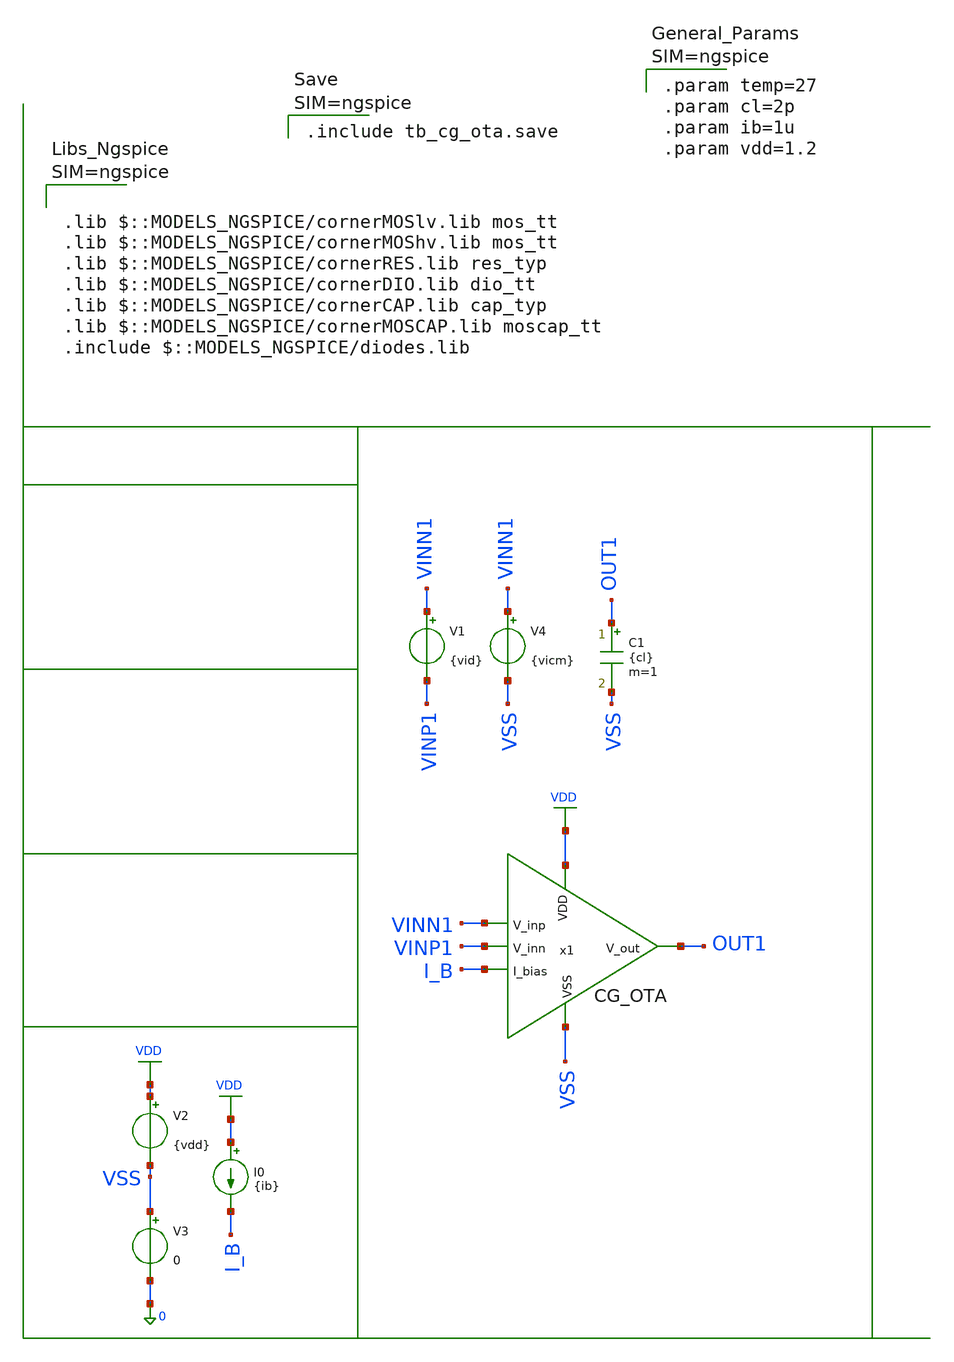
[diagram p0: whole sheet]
** sch_path: designs/libs/tb_analog/tb_cg_ota/tb_cg_ota.sch
**.subckt tb_cg_ota
x1 VDD VINN1 VINP1 OUT1 I_B VSS cg_ota
V1 VINN1 VINP1 {vid}
I0 VDD I_B {ib}
V2 VDD VSS {vdd}
V3 VSS 0 0
V4 VINN1 VSS {vicm}
C1 OUT1 VSS {cl} m=1
**** begin user architecture code


.param temp=27
.param cl=2p
.param ib=1u
.param vdd=1.2





.param vid=0
.param vicm=0.6
.op
.control
save all
op
shell mkdir -p result
run
write ./result/tb_cg_ota_op.raw
show all : vgs, vds, vth
let i_q = -i(v2)
let p_q = i_q * 1.2
let p_q_uw = p_q * 1e6
let i_q_ua = i_q * 1e6
echo "======================================================="
echo " Quiescent Current (I_q): " $&i_q_ua " uA"
echo " Quiescent Power (P_q): " $&p_q_uw " uW"
echo "======================================================="
.endc





.include tb_cg_ota.save







.lib $::MODELS_NGSPICE/cornerMOSlv.lib mos_tt
.lib $::MODELS_NGSPICE/cornerMOShv.lib mos_tt
.lib $::MODELS_NGSPICE/cornerRES.lib res_typ
.lib $::MODELS_NGSPICE/cornerDIO.lib dio_tt
.lib $::MODELS_NGSPICE/cornerCAP.lib cap_typ
.lib $::MODELS_NGSPICE/cornerMOSCAP.lib moscap_tt
.include $::MODELS_NGSPICE/diodes.lib





.param vid=0
.param vicm=0.6
.op
.control
save all
op
shell mkdir -p result
run
write ./result/tb_cg_ota_op.raw
show all : vgs, vds, vth
let i_q = -i(v2)
let p_q = i_q * 1.2
let p_q_uw = p_q * 1e6
let i_q_ua = i_q * 1e6
echo "======================================================="
echo " Quiescent Current (I_q): " $&i_q_ua " uA"
echo " Quiescent Power (P_q): " $&p_q_uw " uW"
echo "======================================================="
.endc





.param vid=0
.param vicm=0.6
.op
.control
save all
op
shell mkdir -p result
run
write ./result/tb_cg_ota_op.raw
show all : vgs, vds, vth
let i_q = -i(v2)
let p_q = i_q * 1.2
let p_q_uw = p_q * 1e6
let i_q_ua = i_q * 1e6
echo "======================================================="
echo " Quiescent Current (I_q): " $&i_q_ua " uA"
echo " Quiescent Power (P_q): " $&p_q_uw " uW"
echo "======================================================="
.endc



**** end user architecture code
**.ends

* expanding   symbol:
*+  /foss/designs/Programmable-Instrumentation-Amplifier-IP/designs/libs/core_analog/coarse_gain/cg_ota.sym # of pins=6
** sym_path: designs/libs/core_analog/coarse_gain/cg_ota.sym
** sch_path: designs/libs/core_analog/coarse_gain/cg_ota.sch
.subckt cg_ota VDD V_inp V_inn V_out I_bias VSS
*.ipin V_inp
*.ipin VDD
*.ipin VSS
*.opin V_out
*.ipin I_bias
*.ipin V_inn
XM1 F1 V_inp net7 net8 sg13_lv_pmos w=26.56u l=2u ng=4 m=1 mm_ok=1
XM2 F2 V_inn net7 net8 sg13_lv_pmos w=26.56u l=2u ng=4 m=1 mm_ok=1
XM3 net1 net1 VDD VDD sg13_lv_pmos w=7.33u l=2u ng=1 m=1 mm_ok=1
XM4 N_A net1 VDD VDD sg13_lv_pmos w=7.33u l=2u ng=1 m=1 mm_ok=1
XM7 F1 V_bn2 VSS VSS sg13_lv_nmos w=9.21u l=2u ng=1 m=1 mm_ok=1
XM8 F2 V_bn2 VSS VSS sg13_lv_nmos w=9.21u l=2u ng=1 m=1 mm_ok=1
XM_tail net7 V_btail VDD VDD sg13_lv_pmos w=5.33u l=2u ng=1 m=4 mm_ok=1
XM_ctrlp N_B V_ctrlp N_A VDD sg13_lv_pmos w=2.20u l=0.50u ng=1 m=1 mm_ok=1
XM_outp V_out N_A VDD VDD sg13_lv_pmos w=22.20u l=0.5u ng=4 m=1 mm_ok=1
XM_ctrln N_A V_ctrln N_B VSS sg13_lv_nmos w=0.84u l=0.5u ng=1 m=1 mm_ok=1
XM_outn V_out N_B VSS VSS sg13_lv_nmos w=8.40u l=0.5u ng=4 m=1 mm_ok=1
XM5 net1 V_bn1 F1 VDD sg13_lv_nmos w=6.41u l=2u ng=1 m=1 mm_ok=1
XM6 N_A V_bn1 F2 VDD sg13_lv_nmos w=6.41u l=2u ng=1 m=1 mm_ok=1
XM_mp1 net2 net2 VDD VDD sg13_lv_pmos w=2.30u l=2u ng=1 m=1 mm_ok=1
XM_mn1 net2 I_bias VSS VSS sg13_lv_nmos w=0.87u l=2u ng=1 m=1 mm_ok=1
XM_refn I_bias I_bias VSS VSS sg13_lv_nmos w=0.87u l=2u ng=1 m=1 mm_ok=1
XM_mp2 V_bn1 net2 VDD VDD sg13_lv_pmos w=11.50u l=2u ng=2 m=1 mm_ok=1
XM_mp3 V_bn2 net2 VDD VDD sg13_lv_pmos w=22.30u l=2u ng=4 m=1 mm_ok=1
XM_bn1 V_bn1 V_bn1 net4 net3 sg13_lv_nmos w=1.60u l=2u ng=1 m=1 mm_ok=1
XM_bn2 V_bn2 V_bn2 VSS VSS sg13_lv_nmos w=9.21u l=2u ng=1 m=1 mm_ok=1
XM_mn2 V_btail I_bias VSS VSS sg13_lv_nmos w=8.7u l=2u ng=1 m=1 mm_ok=1
XM_rep_tail V_btail V_btail VDD VDD sg13_lv_pmos w=5.33u l=2u ng=1 m=4 mm_ok=1
XM_mn4 N_B I_bias VSS VSS sg13_lv_nmos w=2.82u l=2u ng=1 m=1 mm_ok=1
XC1 F2 V_out cap_cmomf w=22.58e-6 l=22.58e-6 mmin=1 mmax=4 subblock=0 rfmodel=0 subscale=1 m=1
+ mm_ok=1
XC2 N_A V_out cap_cmomf w=15.85e-6 l=15.85e-6 mmin=1 mmax=4 subblock=0 rfmodel=0 subscale=1 m=1
+ mm_ok=1
XR1 net4 VSS sub! rhigh w=0.5e-6 l=17e-6 m=1 b=0 mm_ok=1
XM_mp4 V_ctrln net2 VDD VDD sg13_lv_pmos w=3.73u l=2u ng=1 m=1 mm_ok=1
XM_rep_ctrln V_ctrln V_ctrln net5 VSS sg13_lv_nmos w=0.84u l=0.5u ng=1 m=1 mm_ok=1
XM_rep_outn net5 net5 VSS VSS sg13_lv_nmos w=8.40u l=0.5u ng=4 m=1 mm_ok=1
XM_mn3 V_ctrlp I_bias VSS VSS sg13_lv_nmos w=1.41u l=2u ng=1 m=1 mm_ok=1
XM_rep_outp net6 net6 VDD VDD sg13_lv_pmos w=22.20u l=0.5u ng=4 m=1 mm_ok=1
XM_rep_ctrlp V_ctrlp V_ctrlp net6 VDD sg13_lv_pmos w=2.20u l=0.50u ng=1 m=1 mm_ok=1
.ends

.GLOBAL VDD
.end
